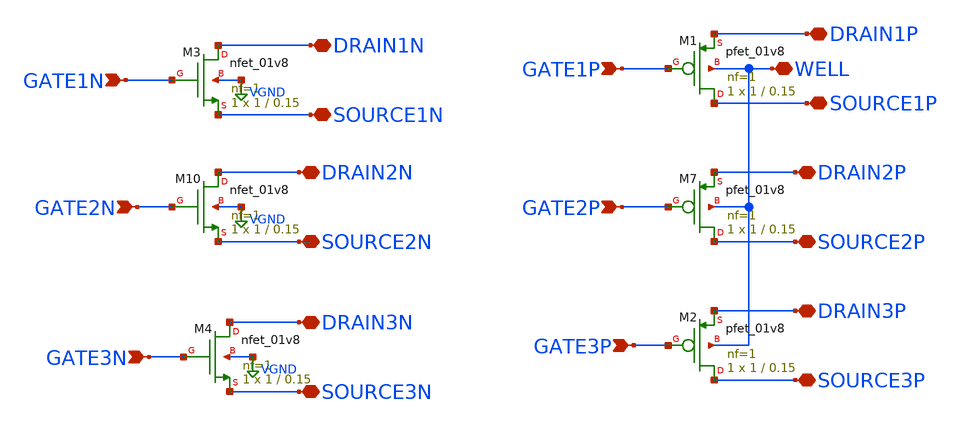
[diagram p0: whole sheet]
** sch_path: libs.ref/sky130_hilas_sc/xschem/sky130_hilas_Trans4small.sch
**.subckt sky130_hilas_Trans4small GATE2N WELL SOURCE2P GATE1N DRAIN1N SOURCE3P GATE3P DRAIN3N
*+ DRAIN2N GATE2P SOURCE1P GATE1P GATE3N DRAIN1P DRAIN3P DRAIN2P SOURCE2N SOURCE3N SOURCE1N
*.ipin GATE2N
*.iopin WELL
*.iopin SOURCE2P
*.ipin GATE1N
*.iopin DRAIN1N
*.iopin SOURCE3P
*.ipin GATE3P
*.iopin DRAIN3N
*.iopin DRAIN2N
*.ipin GATE2P
*.iopin SOURCE1P
*.ipin GATE1P
*.ipin GATE3N
*.iopin DRAIN1P
*.iopin DRAIN3P
*.iopin DRAIN2P
*.iopin SOURCE2N
*.iopin SOURCE3N
*.iopin SOURCE1N
XM1 SOURCE1P GATE1P DRAIN1P WELL sky130_fd_pr__pfet_01v8 L=0.15 W=1 nf=1 ad='int((nf+1)/2) * W/nf * 0.29'
+ as='int((nf+2)/2) * W/nf * 0.29' pd='2*int((nf+1)/2) * (W/nf + 0.29)' ps='2*int((nf+2)/2) * (W/nf + 0.29)'
+ nrd='0.29 / W' nrs='0.29 / W' sa=0 sb=0 sd=0 mult=1 m=1
XM2 SOURCE3P GATE3P DRAIN3P WELL sky130_fd_pr__pfet_01v8 L=0.15 W=1 nf=1 ad='int((nf+1)/2) * W/nf * 0.29'
+ as='int((nf+2)/2) * W/nf * 0.29' pd='2*int((nf+1)/2) * (W/nf + 0.29)' ps='2*int((nf+2)/2) * (W/nf + 0.29)'
+ nrd='0.29 / W' nrs='0.29 / W' sa=0 sb=0 sd=0 mult=1 m=1
XM3 DRAIN1N GATE1N SOURCE1N VGND sky130_fd_pr__nfet_01v8 L=0.15 W=1 nf=1 ad='int((nf+1)/2) * W/nf * 0.29'
+ as='int((nf+2)/2) * W/nf * 0.29' pd='2*int((nf+1)/2) * (W/nf + 0.29)' ps='2*int((nf+2)/2) * (W/nf + 0.29)'
+ nrd='0.29 / W' nrs='0.29 / W' sa=0 sb=0 sd=0 mult=1 m=1
XM4 DRAIN3N GATE3N SOURCE3N VGND sky130_fd_pr__nfet_01v8 L=0.15 W=1 nf=1 ad='int((nf+1)/2) * W/nf * 0.29'
+ as='int((nf+2)/2) * W/nf * 0.29' pd='2*int((nf+1)/2) * (W/nf + 0.29)' ps='2*int((nf+2)/2) * (W/nf + 0.29)'
+ nrd='0.29 / W' nrs='0.29 / W' sa=0 sb=0 sd=0 mult=1 m=1
XM7 SOURCE2P GATE2P DRAIN2P WELL sky130_fd_pr__pfet_01v8 L=0.15 W=1 nf=1 ad='int((nf+1)/2) * W/nf * 0.29'
+ as='int((nf+2)/2) * W/nf * 0.29' pd='2*int((nf+1)/2) * (W/nf + 0.29)' ps='2*int((nf+2)/2) * (W/nf + 0.29)'
+ nrd='0.29 / W' nrs='0.29 / W' sa=0 sb=0 sd=0 mult=1 m=1
XM10 DRAIN2N GATE2N SOURCE2N VGND sky130_fd_pr__nfet_01v8 L=0.15 W=1 nf=1 ad='int((nf+1)/2) * W/nf * 0.29'
+ as='int((nf+2)/2) * W/nf * 0.29' pd='2*int((nf+1)/2) * (W/nf + 0.29)' ps='2*int((nf+2)/2) * (W/nf + 0.29)'
+ nrd='0.29 / W' nrs='0.29 / W' sa=0 sb=0 sd=0 mult=1 m=1
**.ends
.GLOBAL VGND
.end
